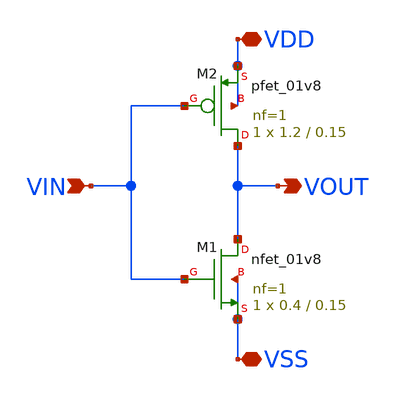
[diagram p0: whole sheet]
** sch_path: xschem/DC_DC_Converter_xschem/DC_DC_Converter/Delay_block_revised/Inverter_0/Inverter0.sch
**.subckt Inverter0 VIN VDD VSS VOUT
*.ipin VIN
*.iopin VDD
*.iopin VSS
*.opin VOUT
XM1 VOUT VIN VSS VSS sky130_fd_pr__nfet_01v8 L=0.15 W=0.4 nf=1 ad='int((nf+1)/2) * W/nf * 0.29' as='int((nf+2)/2) * W/nf * 0.29'
+ pd='2*int((nf+1)/2) * (W/nf + 0.29)' ps='2*int((nf+2)/2) * (W/nf + 0.29)' nrd='0.29 / W' nrs='0.29 / W'
+ sa=0 sb=0 sd=0 mult=1 m=1
XM2 VOUT VIN VDD VDD sky130_fd_pr__pfet_01v8 L=0.15 W=1.2 nf=1 ad='int((nf+1)/2) * W/nf * 0.29' as='int((nf+2)/2) * W/nf * 0.29'
+ pd='2*int((nf+1)/2) * (W/nf + 0.29)' ps='2*int((nf+2)/2) * (W/nf + 0.29)' nrd='0.29 / W' nrs='0.29 / W'
+ sa=0 sb=0 sd=0 mult=1 m=1
**.ends
.end
